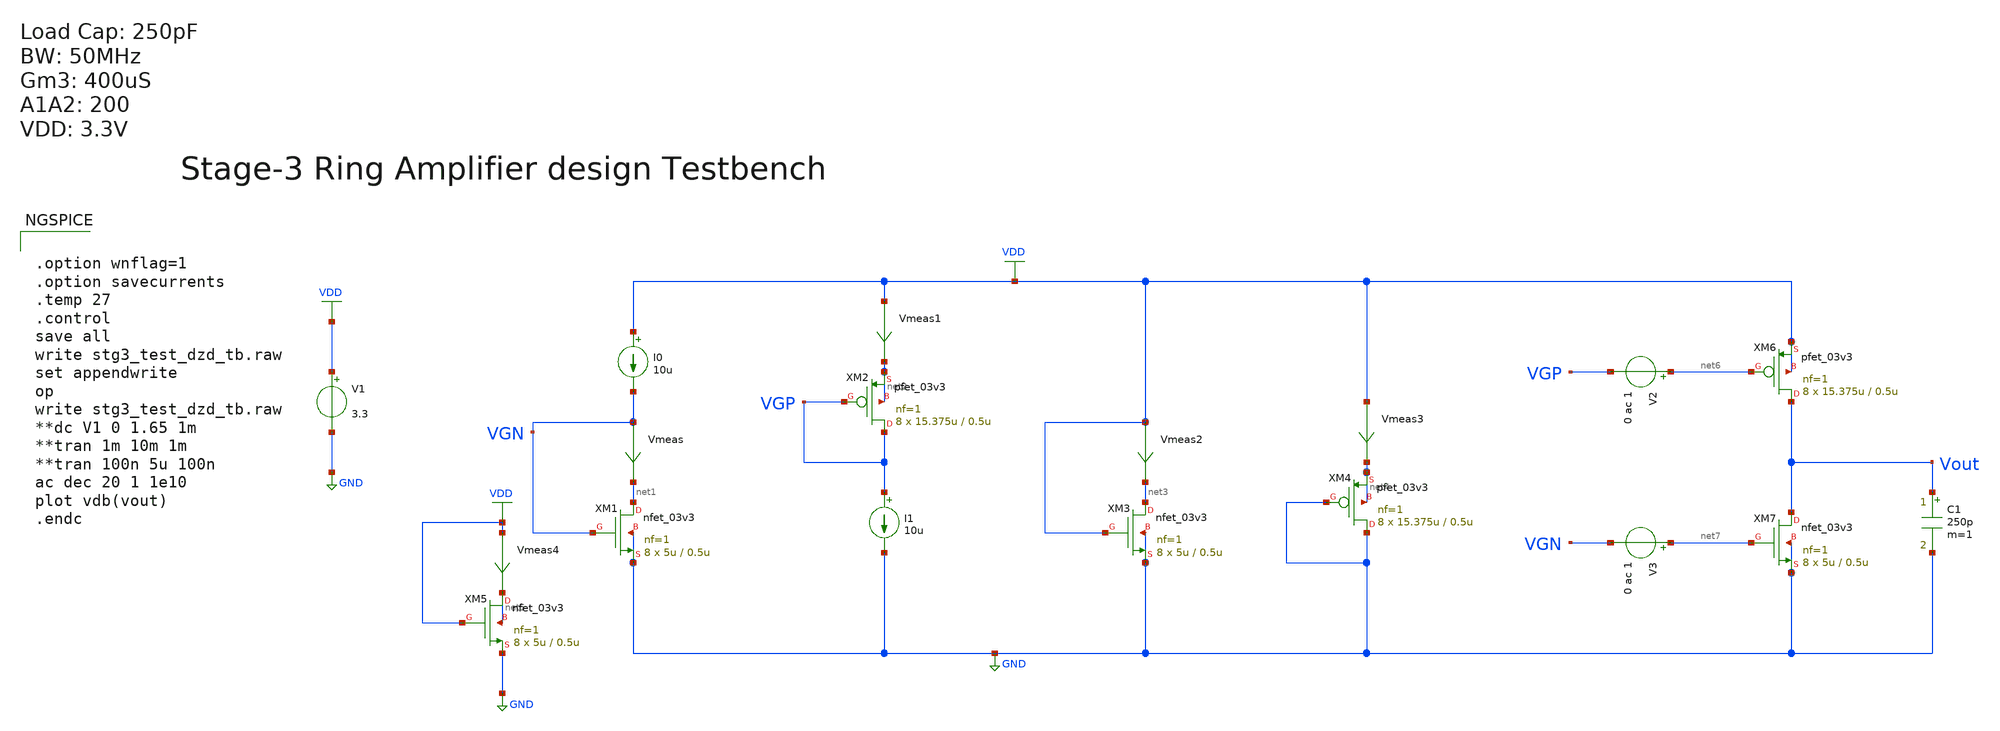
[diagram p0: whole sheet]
** sch_path: Design_Files/Ring-amp/STG3/stg3_test_dzd_tb.sch
**.subckt stg3_test_dzd_tb
XM1 net1 VGN GND GND nfet_03v3 L=0.5u W=5u nf=1 ad='int((nf+1)/2) * W/nf * 0.18u' as='int((nf+2)/2) * W/nf * 0.18u'
+ pd='2*int((nf+1)/2) * (W/nf + 0.18u)' ps='2*int((nf+2)/2) * (W/nf + 0.18u)' nrd='0.18u / W' nrs='0.18u / W'
+ sa=0 sb=0 sd=0 m=8
I0 VDD VGN 10u
V1 VDD GND 3.3
Vmeas VGN net1 0
.save i(vmeas)
XM2 VGP VGP net2 net2 pfet_03v3 L=0.5u W=15.375u nf=1 ad='int((nf+1)/2) * W/nf * 0.18u' as='int((nf+2)/2) * W/nf * 0.18u'
+ pd='2*int((nf+1)/2) * (W/nf + 0.18u)' ps='2*int((nf+2)/2) * (W/nf + 0.18u)' nrd='0.18u / W' nrs='0.18u / W'
+ sa=0 sb=0 sd=0 m=8
I1 VGP GND 10u
Vmeas1 VDD net2 0
.save i(vmeas1)
XM3 net3 VDD GND GND nfet_03v3 L=0.5u W=5u nf=1 ad='int((nf+1)/2) * W/nf * 0.18u' as='int((nf+2)/2) * W/nf * 0.18u'
+ pd='2*int((nf+1)/2) * (W/nf + 0.18u)' ps='2*int((nf+2)/2) * (W/nf + 0.18u)' nrd='0.18u / W' nrs='0.18u / W'
+ sa=0 sb=0 sd=0 m=8
Vmeas2 VDD net3 0
.save i(vmeas2)
XM4 GND GND net4 net4 pfet_03v3 L=0.5u W=15.375u nf=1 ad='int((nf+1)/2) * W/nf * 0.18u' as='int((nf+2)/2) * W/nf * 0.18u'
+ pd='2*int((nf+1)/2) * (W/nf + 0.18u)' ps='2*int((nf+2)/2) * (W/nf + 0.18u)' nrd='0.18u / W' nrs='0.18u / W'
+ sa=0 sb=0 sd=0 m=8
Vmeas3 VDD net4 0
.save i(vmeas3)
XM5 net5 VDD GND net5 nfet_03v3 L=0.5u W=5u nf=1 ad='int((nf+1)/2) * W/nf * 0.18u' as='int((nf+2)/2) * W/nf * 0.18u'
+ pd='2*int((nf+1)/2) * (W/nf + 0.18u)' ps='2*int((nf+2)/2) * (W/nf + 0.18u)' nrd='0.18u / W' nrs='0.18u / W'
+ sa=0 sb=0 sd=0 m=8
Vmeas4 VDD net5 0
.save i(vmeas4)
XM6 Vout net6 VDD VDD pfet_03v3 L=0.5u W=15.375u nf=1 ad='int((nf+1)/2) * W/nf * 0.18u' as='int((nf+2)/2) * W/nf * 0.18u'
+ pd='2*int((nf+1)/2) * (W/nf + 0.18u)' ps='2*int((nf+2)/2) * (W/nf + 0.18u)' nrd='0.18u / W' nrs='0.18u / W'
+ sa=0 sb=0 sd=0 m=8
XM7 Vout net7 GND GND nfet_03v3 L=0.5u W=5u nf=1 ad='int((nf+1)/2) * W/nf * 0.18u' as='int((nf+2)/2) * W/nf * 0.18u'
+ pd='2*int((nf+1)/2) * (W/nf + 0.18u)' ps='2*int((nf+2)/2) * (W/nf + 0.18u)' nrd='0.18u / W' nrs='0.18u / W'
+ sa=0 sb=0 sd=0 m=8
V2 net6 VGP 0 ac 1
V3 net7 VGN 0 ac 1
C1 Vout GND 250p m=1
**** begin user architecture code


.option wnflag=1
.option savecurrents
.temp 27
.control
save all
write stg3_test_dzd_tb.raw
set appendwrite
op
write stg3_test_dzd_tb.raw
**dc V1 0 1.65 1m
**tran 1m 10m 1m
**tran 100n 5u 100n
ac dec 20 1 1e10
plot vdb(vout)
.endc




.lib /foss/pdks/volare/gf180mcu/versions/0fe599b2afb6708d281543108caf8310912f54af/gf180mcuD/libs.tech/ngspice/sm141064.ngspice typical
.include /foss/pdks/volare/gf180mcu/versions/0fe599b2afb6708d281543108caf8310912f54af/gf180mcuD/libs.tech/ngspice/design.ngspice

*.include $::180MCU_MODELS/design.ngspice
*.lib $::180MCU_MODELS/sm141064.ngspice typical




.save @m.xm1.m0[gm]
.save @m.xm1.m0[id]
.save @m.xm1.m0[vth]
.save @m.xm1.m0[gds]
.save @m.xm1.m0[cgg]
.save @m.xm1.m0[cgs]
.save @m.xm1.m0[cgd]
.save @m.xm2.m0[gm]
.save @m.xm2.m0[id]
.save @m.xm2.m0[vth]
.save @m.xm2.m0[gds]
.save @m.xm2.m0[cgg]
.save @m.xm2.m0[cgs]
.save @m.xm2.m0[cgd]
.save @m.xm3.m0[gm]
.save @m.xm3.m0[id]
.save @m.xm3.m0[vth]
.save @m.xm3.m0[vds]
.save @m.xm3.m0[gds]
.save @m.xm3.m0[cgg]
.save @m.xm3.m0[cgs]
.save @m.xm3.m0[cgd]
.save @m.xm4.m0[gm]
.save @m.xm4.m0[id]
.save @m.xm4.m0[vth]
.save @m.xm4.m0[vds]
.save @m.xm4.m0[gds]
.save @m.xm4.m0[cgg]
.save @m.xm4.m0[cgs]
.save @m.xm4.m0[cgd]


**** end user architecture code
**.ends
.GLOBAL GND
.GLOBAL VDD
.end
